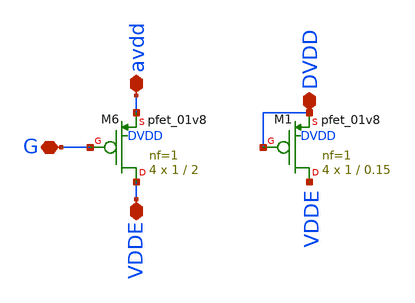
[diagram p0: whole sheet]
** sch_path: magic/pmos_ena.sch
**.subckt pmos_ena G avdd VDDE DVDD
*.iopin G
*.iopin avdd
*.iopin VDDE
*.iopin DVDD
XM6 VDDE G avdd DVDD sky130_fd_pr__pfet_01v8 L=2 W=1 nf=1 ad='int((nf+1)/2) * W/nf * 0.29' as='int((nf+2)/2) * W/nf * 0.29'
+ pd='2*int((nf+1)/2) * (W/nf + 0.29)' ps='2*int((nf+2)/2) * (W/nf + 0.29)' nrd='0.29 / W' nrs='0.29 / W'
+ sa=0 sb=0 sd=0 mult=4 m=4
XM1 VDDE DVDD DVDD DVDD sky130_fd_pr__pfet_01v8 L=0.15 W=1 nf=1 ad='int((nf+1)/2) * W/nf * 0.29' as='int((nf+2)/2) * W/nf * 0.29'
+ pd='2*int((nf+1)/2) * (W/nf + 0.29)' ps='2*int((nf+2)/2) * (W/nf + 0.29)' nrd='0.29 / W' nrs='0.29 / W'
+ sa=0 sb=0 sd=0 mult=4 m=4
**.ends
.end
